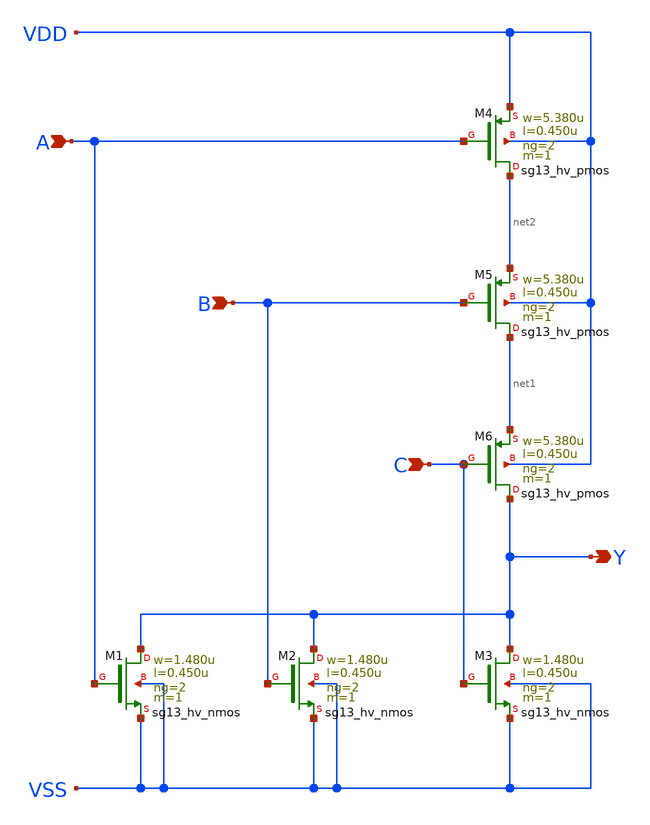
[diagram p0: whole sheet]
** sch_path: ihp-sg13g2/libs.ref/sg13g2_stdcell_hv/sch/xschem/sg13g2_hv_nor3_2.sch
* Copyright 2023 IHP PDK Authors
* Licensed under the Apache License, Version 2.0 (the "License");
* you may not use this file except in compliance with the License.
* You may obtain a copy of the License at
* https://www.apache.org/licenses/LICENSE-2.0
* Unless required by applicable law or agreed to in writing, software
* distributed under the License is distributed on an "AS IS" BASIS,
* WITHOUT WARRANTIES OR CONDITIONS OF ANY KIND, either express or implied.
* See the License for the specific language governing permissions and
* limitations under the License.
**.subckt sg13g2_hv_nor3_2 B Y A C
*.ipin B
*.opin Y
*.ipin A
*.ipin C
XM1 Y A VSS VSS sg13_hv_nmos w=1.480u l=0.450u ng=2 m=1 mm_ok=1
XM2 Y B VSS VSS sg13_hv_nmos w=1.480u l=0.450u ng=2 m=1 mm_ok=1
XM3 Y C VSS VSS sg13_hv_nmos w=1.480u l=0.450u ng=2 m=1 mm_ok=1
XM4 net2 A VDD VDD sg13_hv_pmos w=5.380u l=0.450u ng=2 m=1 mm_ok=1
XM5 net1 B net2 VDD sg13_hv_pmos w=5.380u l=0.450u ng=2 m=1 mm_ok=1
XM6 Y C net1 VDD sg13_hv_pmos w=5.380u l=0.450u ng=2 m=1 mm_ok=1
**.ends
.end
